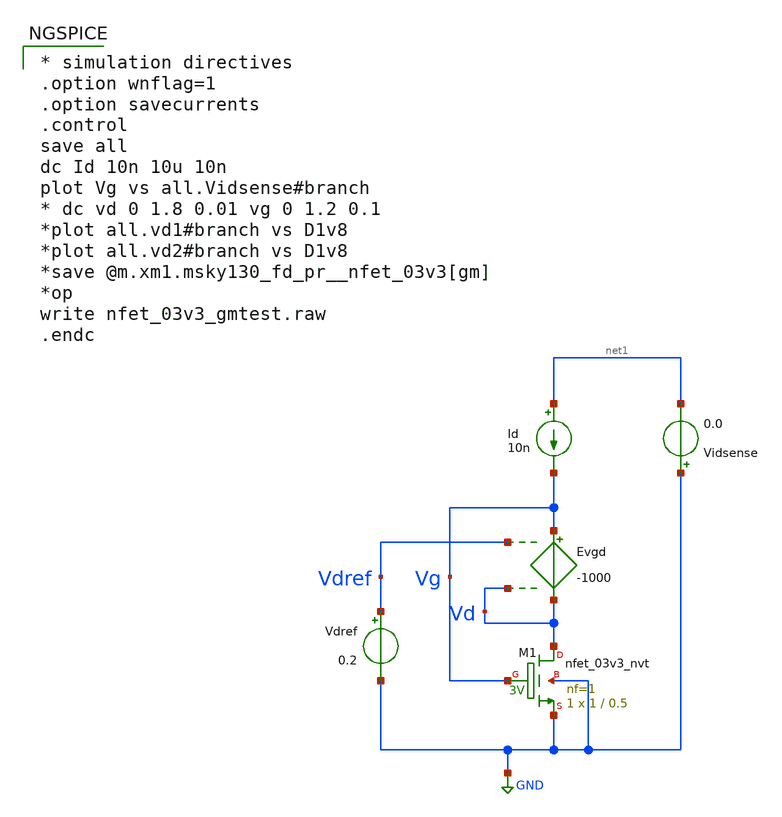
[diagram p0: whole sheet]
** sch_path: playground/nfet_03v3_gmtest.sch
**.subckt nfet_03v3_gmtest
XM1 Vd Vg GND GND sky130_fd_pr__nfet_03v3_nvt L=0.5 W=1 nf=1 ad='int((nf+1)/2) * W/nf * 0.29' as='int((nf+2)/2) * W/nf * 0.29'
+ pd='2*int((nf+1)/2) * (W/nf + 0.29)' ps='2*int((nf+2)/2) * (W/nf + 0.29)' nrd='0.29 / W' nrs='0.29 / W'
+ sa=0 sb=0 sd=0 mult=1 m=1
Evgd Vg Vd Vdref Vd -1000
Id net1 Vg 10n
Vdref Vdref GND 0.2
Vidsense GND net1 0.0
**** begin user architecture code

.include $::SKYWATER_MODELS/cells/nfet_01v8/sky130_fd_pr__nfet_01v8__tt.corner.spice
.include $::SKYWATER_MODELS/cells/nfet_01v8_lvt/sky130_fd_pr__nfet_01v8_lvt__tt.corner.spice
.include $::SKYWATER_MODELS/cells/pfet_01v8/sky130_fd_pr__pfet_01v8__tt.corner.spice
.include $::SKYWATER_MODELS/cells/nfet_03v3_nvt/sky130_fd_pr__nfet_03v3_nvt__tt.corner.spice
.include $::SKYWATER_MODELS/cells/nfet_05v0_nvt/sky130_fd_pr__nfet_05v0_nvt__tt.corner.spice
.include $::SKYWATER_MODELS/cells/esd_nfet_01v8/sky130_fd_pr__esd_nfet_01v8__tt.corner.spice
.include $::SKYWATER_MODELS/cells/pfet_01v8_lvt/sky130_fd_pr__pfet_01v8_lvt__tt.corner.spice
.include $::SKYWATER_MODELS/cells/pfet_01v8_hvt/sky130_fd_pr__pfet_01v8_hvt__tt.corner.spice
.include $::SKYWATER_MODELS/cells/esd_pfet_g5v0d10v5/sky130_fd_pr__esd_pfet_g5v0d10v5__tt.corner.spice
.include $::SKYWATER_MODELS/cells/pfet_g5v0d10v5/sky130_fd_pr__pfet_g5v0d10v5__tt.corner.spice
.include $::SKYWATER_MODELS/cells/pfet_g5v0d16v0/sky130_fd_pr__pfet_g5v0d16v0__tt.corner.spice
.include $::SKYWATER_MODELS/cells/nfet_g5v0d10v5/sky130_fd_pr__nfet_g5v0d10v5__tt.corner.spice
.include $::SKYWATER_MODELS/cells/nfet_g5v0d16v0/sky130_fd_pr__nfet_g5v0d16v0__tt_discrete.corner.spice
.include $::SKYWATER_MODELS/cells/esd_nfet_g5v0d10v5/sky130_fd_pr__esd_nfet_g5v0d10v5__tt.corner.spice
.include $::SKYWATER_MODELS/models/corners/tt/nonfet.spice
* Mismatch parameters
.include $::SKYWATER_MODELS/cells/nfet_01v8/sky130_fd_pr__nfet_01v8__mismatch.corner.spice
.include $::SKYWATER_MODELS/cells/pfet_01v8/sky130_fd_pr__pfet_01v8__mismatch.corner.spice
.include $::SKYWATER_MODELS/cells/nfet_01v8_lvt/sky130_fd_pr__nfet_01v8_lvt__mismatch.corner.spice
.include $::SKYWATER_MODELS/cells/pfet_01v8_lvt/sky130_fd_pr__pfet_01v8_lvt__mismatch.corner.spice
.include $::SKYWATER_MODELS/cells/pfet_01v8_hvt/sky130_fd_pr__pfet_01v8_hvt__mismatch.corner.spice
.include $::SKYWATER_MODELS/cells/nfet_g5v0d10v5/sky130_fd_pr__nfet_g5v0d10v5__mismatch.corner.spice
.include $::SKYWATER_MODELS/cells/pfet_g5v0d10v5/sky130_fd_pr__pfet_g5v0d10v5__mismatch.corner.spice
.include $::SKYWATER_MODELS/cells/nfet_05v0_nvt/sky130_fd_pr__nfet_05v0_nvt__mismatch.corner.spice
.include $::SKYWATER_MODELS/cells/nfet_03v3_nvt/sky130_fd_pr__nfet_03v3_nvt__mismatch.corner.spice
* Resistor$::SKYWATER_MODELS/Capacitor
.include $::SKYWATER_MODELS/models/r+c/res_typical__cap_typical.spice
.include $::SKYWATER_MODELS/models/r+c/res_typical__cap_typical__lin.spice
* Special cells
.include $::SKYWATER_MODELS/models/corners/tt/specialized_cells.spice
* All models
.include $::SKYWATER_MODELS/models/all.spice
* Corner
.include $::SKYWATER_MODELS/models/corners/tt/rf.spice


.include $::SKYWATER_MODELS/cells/nfet_20v0/sky130_fd_pr__nfet_20v0__tt_discrete.corner.spice


* simulation directives
.option wnflag=1
.option savecurrents
.control
save all
dc Id 10n 10u 10n
plot Vg vs all.Vidsense#branch
* dc vd 0 1.8 0.01 vg 0 1.2 0.1
*plot all.vd1#branch vs D1v8
*plot all.vd2#branch vs D1v8
*save @m.xm1.msky130_fd_pr__nfet_03v3[gm]
*op
write nfet_03v3_gmtest.raw
.endc


**** end user architecture code
**.ends
.GLOBAL GND
.end
